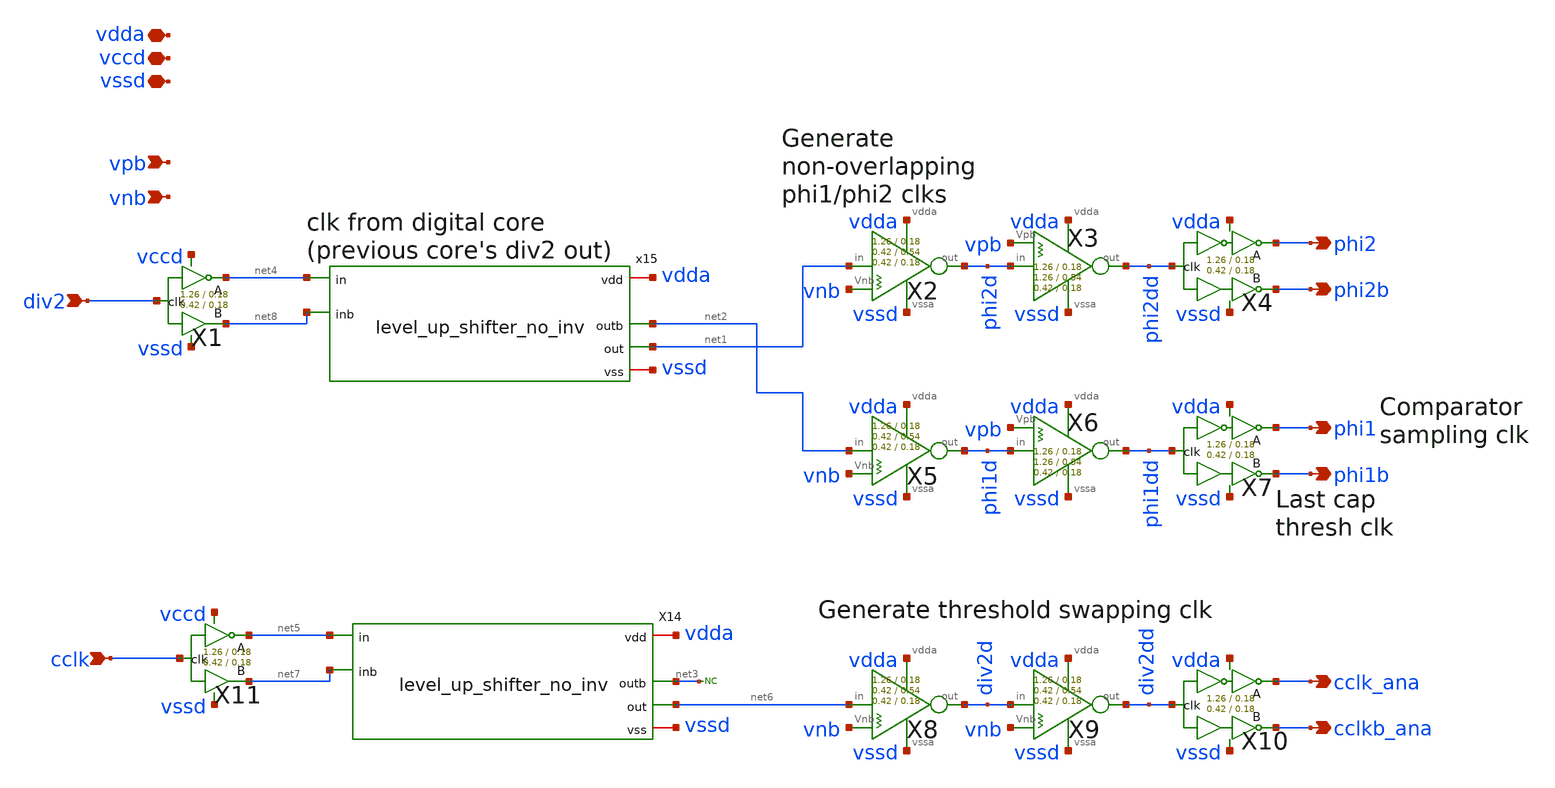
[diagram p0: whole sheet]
** sch_path: xschem/clkgen/filter_clkgen_balanced_clks.sch
**.subckt filter_clkgen_balanced_clks div2 phi2 phi2b phi1 phi1b cclk_ana cclkb_ana vpb vnb cclk
*+ vdda vccd vssd
*.ipin div2
*.opin phi2
*.opin phi2b
*.opin phi1
*.opin phi1b
*.opin cclk_ana
*.opin cclkb_ana
*.ipin vpb
*.ipin vnb
*.ipin cclk
*.iopin vdda
*.iopin vccd
*.iopin vssd
X4 phi2dd phi2 phi2b vdda vssd comp_clks Wpmos=1.26 Lpmos=0.18 Wnmos=0.42 Lnmos=0.18
X7 phi1dd phi1 phi1b vdda vssd comp_clks Wpmos=1.26 Lpmos=0.18 Wnmos=0.42 Lnmos=0.18
X10 div2dd cclk_ana cclkb_ana vdda vssd comp_clks Wpmos=1.26 Lpmos=0.18 Wnmos=0.42 Lnmos=0.18
X1 div2 net4 net8 vccd vssd comp_clks_1stage Wpmos=1.26 Lpmos=0.18 Wnmos=0.42 Lnmos=0.18
X2 net1 phi2d vnb vdda vssd inv_weak_pulldown Wpmos=1.26 Lpmos= Wnmos= Lnmos=0.54
X5 net2 phi1d vnb vdda vssd inv_weak_pulldown Wpmos=1.26 Lpmos= Wnmos= Lnmos=0.54
X8 net6 div2d vnb vdda vssd inv_weak_pulldown Wpmos=1.26 Lpmos= Wnmos= Lnmos=0.54
X9 div2d div2dd vnb vdda vssd inv_weak_pulldown Wpmos=1.26 Lpmos= Wnmos= Lnmos=0.54
X3 phi2d phi2dd vpb vdda vssd inv_weak_pullup Wpmos=1.26 Lpmos=0.54 Wnmos= Lnmos=
X6 phi1d phi1dd vpb vdda vssd inv_weak_pullup Wpmos=1.26 Lpmos=0.54 Wnmos= Lnmos=
X11 cclk net5 net7 vccd vssd comp_clks_1stage Wpmos=1.26 Lpmos=0.18 Wnmos=0.42 Lnmos=0.18
x15 vdda net4 net2 net1 vssd net8 level_up_shifter_no_inv
X14 vdda net5 net3 net6 vssd net7 level_up_shifter_no_inv
* noconn #net3
**.ends
.end
